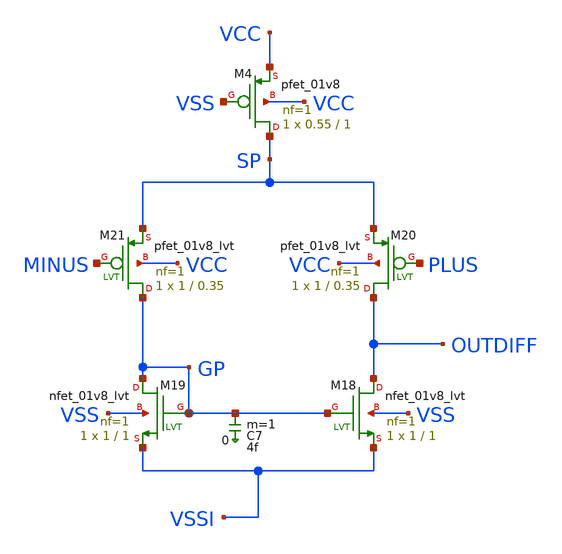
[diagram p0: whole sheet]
** sch_path: idealComp.sch
**.subckt idealComp
C7 GP 0 4f m=1
XM4 SP VSS VCC VCC sky130_fd_pr__pfet_01v8 L=1 W=0.55 nf=1 ad='W * 0.29' as='W * 0.29' pd='W + 2 * 0.29'
+ ps='W + 2 * 0.29' nrd=0 nrs=0 sa=0 sb=0 sd=0 mult=1 m=1
XM18 OUTDIFF GP VSSI VSS sky130_fd_pr__nfet_01v8_lvt L=1 W=1 nf=1 ad='W * 0.29' as='W * 0.29' pd='2*(W + 0.29)'
+ ps='2*(W + 0.29)' nrd=0 nrs=0 sa=0 sb=0 sd=0 mult=1 m=1
XM19 GP GP VSSI VSS sky130_fd_pr__nfet_01v8_lvt L=1 W=1 nf=1 ad='W * 0.29' as='W * 0.29' pd='2*(W + 0.29)'
+ ps='2*(W + 0.29)' nrd=0 nrs=0 sa=0 sb=0 sd=0 mult=1 m=1
XM20 OUTDIFF PLUS SP VCC sky130_fd_pr__pfet_01v8_lvt L=0.35 W=1 nf=1 ad='W * 0.29' as='W * 0.29' pd='2*(W + 0.29)'
+ ps='2*(W + 0.29)' nrd=0 nrs=0 sa=0 sb=0 sd=0 mult=1 m=1
XM21 GP MINUS SP VCC sky130_fd_pr__pfet_01v8_lvt L=0.35 W=1 nf=1 ad='W * 0.29' as='W * 0.29' pd='2*(W + 0.29)'
+ ps='2*(W + 0.29)' nrd=0 nrs=0 sa=0 sb=0 sd=0 mult=1 m=1
**.ends
.end
